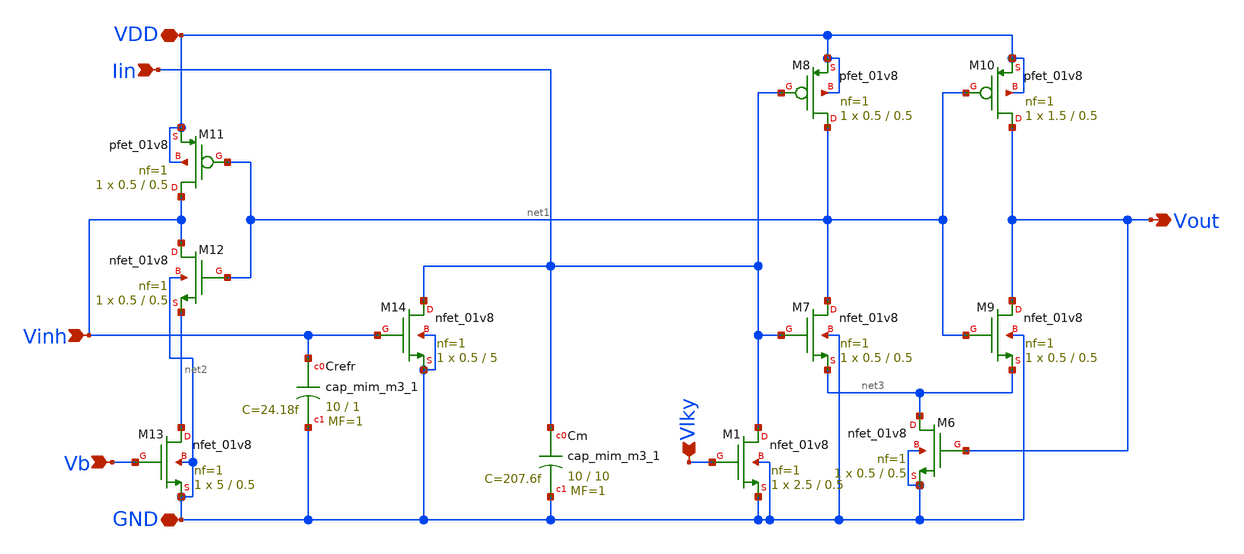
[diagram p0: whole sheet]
** sch_path: LIF_neuron/Output_Layer_LIF.sch
**.subckt Output_Layer_LIF GND Vb VDD Vout Iin Vlky Vinh
*.iopin GND
*.ipin Vb
*.iopin VDD
*.opin Vout
*.ipin Iin
*.ipin Vlky
*.ipin Vinh
XM13 net2 Vb GND GND sky130_fd_pr__nfet_01v8 L=0.5 W=5 nf=1 ad='int((nf+1)/2) * W/nf * 0.29' as='int((nf+2)/2) * W/nf * 0.29'
+ pd='2*int((nf+1)/2) * (W/nf + 0.29)' ps='2*int((nf+2)/2) * (W/nf + 0.29)' nrd='0.29 / W' nrs='0.29 / W'
+ sa=0 sb=0 sd=0 mult=1 m=1
XM12 Vinh net1 net2 GND sky130_fd_pr__nfet_01v8 L=0.5 W=0.5 nf=1 ad='int((nf+1)/2) * W/nf * 0.29' as='int((nf+2)/2) * W/nf * 0.29'
+ pd='2*int((nf+1)/2) * (W/nf + 0.29)' ps='2*int((nf+2)/2) * (W/nf + 0.29)' nrd='0.29 / W' nrs='0.29 / W'
+ sa=0 sb=0 sd=0 mult=1 m=1
XM11 Vinh net1 VDD VDD sky130_fd_pr__pfet_01v8 L=0.5 W=0.5 nf=1 ad='int((nf+1)/2) * W/nf * 0.29' as='int((nf+2)/2) * W/nf * 0.29'
+ pd='2*int((nf+1)/2) * (W/nf + 0.29)' ps='2*int((nf+2)/2) * (W/nf + 0.29)' nrd='0.29 / W' nrs='0.29 / W'
+ sa=0 sb=0 sd=0 mult=1 m=1
XCrefr Vinh GND sky130_fd_pr__cap_mim_m3_1 W=10 L=1 MF=1 m=1
XM14 Iin Vinh GND GND sky130_fd_pr__nfet_01v8 L=5 W=0.5 nf=1 ad='int((nf+1)/2) * W/nf * 0.29' as='int((nf+2)/2) * W/nf * 0.29'
+ pd='2*int((nf+1)/2) * (W/nf + 0.29)' ps='2*int((nf+2)/2) * (W/nf + 0.29)' nrd='0.29 / W' nrs='0.29 / W'
+ sa=0 sb=0 sd=0 mult=1 m=1
XCm Iin GND sky130_fd_pr__cap_mim_m3_1 W=10 L=10 MF=1 m=1
XM6 net3 Vout GND GND sky130_fd_pr__nfet_01v8 L=0.5 W=0.5 nf=1 ad='int((nf+1)/2) * W/nf * 0.29' as='int((nf+2)/2) * W/nf * 0.29'
+ pd='2*int((nf+1)/2) * (W/nf + 0.29)' ps='2*int((nf+2)/2) * (W/nf + 0.29)' nrd='0.29 / W' nrs='0.29 / W'
+ sa=0 sb=0 sd=0 mult=1 m=1
XM7 net1 Iin net3 GND sky130_fd_pr__nfet_01v8 L=0.5 W=0.5 nf=1 ad='int((nf+1)/2) * W/nf * 0.29' as='int((nf+2)/2) * W/nf * 0.29'
+ pd='2*int((nf+1)/2) * (W/nf + 0.29)' ps='2*int((nf+2)/2) * (W/nf + 0.29)' nrd='0.29 / W' nrs='0.29 / W'
+ sa=0 sb=0 sd=0 mult=1 m=1
XM8 net1 Iin VDD VDD sky130_fd_pr__pfet_01v8 L=0.5 W=0.5 nf=1 ad='int((nf+1)/2) * W/nf * 0.29' as='int((nf+2)/2) * W/nf * 0.29'
+ pd='2*int((nf+1)/2) * (W/nf + 0.29)' ps='2*int((nf+2)/2) * (W/nf + 0.29)' nrd='0.29 / W' nrs='0.29 / W'
+ sa=0 sb=0 sd=0 mult=1 m=1
XM9 Vout net1 net3 GND sky130_fd_pr__nfet_01v8 L=0.5 W=0.5 nf=1 ad='int((nf+1)/2) * W/nf * 0.29' as='int((nf+2)/2) * W/nf * 0.29'
+ pd='2*int((nf+1)/2) * (W/nf + 0.29)' ps='2*int((nf+2)/2) * (W/nf + 0.29)' nrd='0.29 / W' nrs='0.29 / W'
+ sa=0 sb=0 sd=0 mult=1 m=1
XM10 Vout net1 VDD VDD sky130_fd_pr__pfet_01v8 L=0.5 W=1.5 nf=1 ad='int((nf+1)/2) * W/nf * 0.29' as='int((nf+2)/2) * W/nf * 0.29'
+ pd='2*int((nf+1)/2) * (W/nf + 0.29)' ps='2*int((nf+2)/2) * (W/nf + 0.29)' nrd='0.29 / W' nrs='0.29 / W'
+ sa=0 sb=0 sd=0 mult=1 m=1
XM1 Iin Vlky GND GND sky130_fd_pr__nfet_01v8 L=0.5 W=2.5 nf=1 ad='int((nf+1)/2) * W/nf * 0.29' as='int((nf+2)/2) * W/nf * 0.29'
+ pd='2*int((nf+1)/2) * (W/nf + 0.29)' ps='2*int((nf+2)/2) * (W/nf + 0.29)' nrd='0.29 / W' nrs='0.29 / W'
+ sa=0 sb=0 sd=0 mult=1 m=1
**.ends
.end
